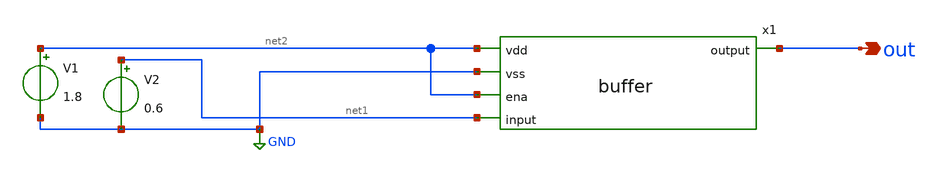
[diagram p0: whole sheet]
** sch_path: xschem/buffer_tb.sch
**.subckt buffer_tb out
*.opin out
V1 net2 GND 1.8
V2 net1 GND 0.6
x1 net2 GND net2 net1 out buffer
**** begin user architecture code

.lib /usr/local/share/pdk/sky130A/libs.tech/ngspice/sky130.lib.spice tt



.control
option TEMP=25
op
*** DEBUG - search for linear mode trasistor
set altshow
show > /tmp/tras.txt

dc V2 0 1.8 0.05
plot out

.endc

**** end user architecture code
**.ends

* expanding   symbol:  xschem/buffer.sym # of pins=5
** sym_path: xschem/buffer.sym
** sch_path: xschem/buffer.sch
.subckt buffer vdd vss ena input output
*.opin output
*.ipin input
*.ipin vdd
*.ipin vss
*.ipin ena
XM1 net2 input net1 vss sky130_fd_pr__nfet_01v8 L=1 W=1 nf=1 ad='int((nf+1)/2) * W/nf * 0.29' as='int((nf+2)/2) * W/nf * 0.29'
+ pd='2*int((nf+1)/2) * (W/nf + 0.29)' ps='2*int((nf+2)/2) * (W/nf + 0.29)' nrd='0.29 / W' nrs='0.29 / W'
+ sa=0 sb=0 sd=0 mult=1 m=1
XM2 output output net1 vss sky130_fd_pr__nfet_01v8 L=1 W=1 nf=1 ad='int((nf+1)/2) * W/nf * 0.29' as='int((nf+2)/2) * W/nf * 0.29'
+ pd='2*int((nf+1)/2) * (W/nf + 0.29)' ps='2*int((nf+2)/2) * (W/nf + 0.29)' nrd='0.29 / W' nrs='0.29 / W'
+ sa=0 sb=0 sd=0 mult=1 m=1
XM5 net1 ena vss vss sky130_fd_pr__nfet_01v8 L=1 W=1 nf=1 ad='int((nf+1)/2) * W/nf * 0.29' as='int((nf+2)/2) * W/nf * 0.29'
+ pd='2*int((nf+1)/2) * (W/nf + 0.29)' ps='2*int((nf+2)/2) * (W/nf + 0.29)' nrd='0.29 / W' nrs='0.29 / W'
+ sa=0 sb=0 sd=0 mult=1 m=1
XM4 output net2 vdd vdd sky130_fd_pr__pfet_01v8 L=1 W=1 nf=1 ad='int((nf+1)/2) * W/nf * 0.29' as='int((nf+2)/2) * W/nf * 0.29'
+ pd='2*int((nf+1)/2) * (W/nf + 0.29)' ps='2*int((nf+2)/2) * (W/nf + 0.29)' nrd='0.29 / W' nrs='0.29 / W'
+ sa=0 sb=0 sd=0 mult=1 m=1
XM3 net2 net2 vdd vdd sky130_fd_pr__pfet_01v8 L=1 W=1 nf=1 ad='int((nf+1)/2) * W/nf * 0.29' as='int((nf+2)/2) * W/nf * 0.29'
+ pd='2*int((nf+1)/2) * (W/nf + 0.29)' ps='2*int((nf+2)/2) * (W/nf + 0.29)' nrd='0.29 / W' nrs='0.29 / W'
+ sa=0 sb=0 sd=0 mult=1 m=1
.ends

.GLOBAL GND
.end
